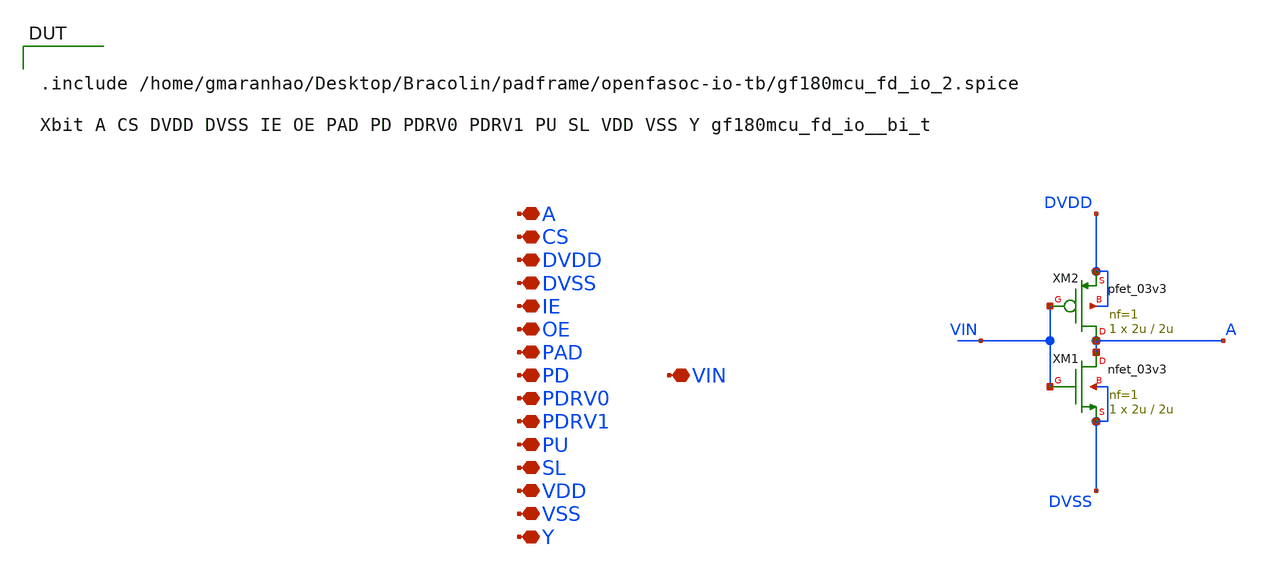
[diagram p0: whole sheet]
** sch_path: padframe/IO_Cells_test/inverter_PAD.sch
**.subckt inverter_PAD A CS DVDD DVSS IE OE PAD PD PDRV0 PDRV1 PU SL VDD VSS Y VIN
*.iopin A
*.iopin CS
*.iopin DVDD
*.iopin DVSS
*.iopin IE
*.iopin OE
*.iopin PAD
*.iopin PD
*.iopin PDRV0
*.iopin PDRV1
*.iopin PU
*.iopin SL
*.iopin VDD
*.iopin VSS
*.iopin Y
*.iopin VIN
XM1 A VIN DVSS DVSS nfet_03v3 L=2u W=2u nf=1 ad='int((nf+1)/2) * W/nf * 0.18u' as='int((nf+2)/2) * W/nf * 0.18u'
+ pd='2*int((nf+1)/2) * (W/nf + 0.18u)' ps='2*int((nf+2)/2) * (W/nf + 0.18u)' nrd='0.18u / W' nrs='0.18u / W'
+ sa=0 sb=0 sd=0 m=1
XM2 A VIN DVDD DVDD pfet_03v3 L=2u W=2u nf=1 ad='int((nf+1)/2) * W/nf * 0.18u' as='int((nf+2)/2) * W/nf * 0.18u'
+ pd='2*int((nf+1)/2) * (W/nf + 0.18u)' ps='2*int((nf+2)/2) * (W/nf + 0.18u)' nrd='0.18u / W' nrs='0.18u / W'
+ sa=0 sb=0 sd=0 m=1
**** begin user architecture code

.include /home/gmaranhao/Desktop/Bracolin/padframe/openfasoc-io-tb/gf180mcu_fd_io_2.spice

Xbit A CS DVDD DVSS IE OE PAD PD PDRV0 PDRV1 PU SL VDD VSS Y gf180mcu_fd_io__bi_t




**** end user architecture code
**.ends
.end
